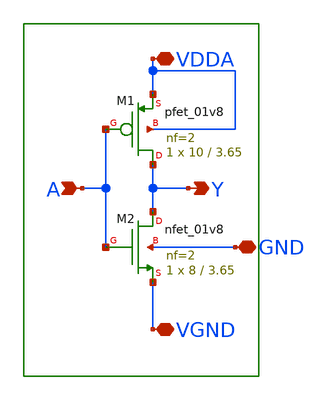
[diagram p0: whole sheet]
** sch_path: xschem/lib/main_inv.sch
**.subckt main_inv VDDA VGND A Y GND
*.iopin VDDA
*.iopin VGND
*.ipin A
*.opin Y
*.iopin GND
XM2 Y A VGND GND sky130_fd_pr__nfet_01v8 L=3.65 W=8 nf=2 ad='int((nf+1)/2) * W/nf * 0.29' as='int((nf+2)/2) * W/nf * 0.29'
+ pd='2*int((nf+1)/2) * (W/nf + 0.29)' ps='2*int((nf+2)/2) * (W/nf + 0.29)' nrd='0.29 / W' nrs='0.29 / W'
+ sa=0 sb=0 sd=0 mult=1 m=1
XM1 Y A VDDA VDDA sky130_fd_pr__pfet_01v8 L=3.65 W=10 nf=2 ad='int((nf+1)/2) * W/nf * 0.29' as='int((nf+2)/2) * W/nf * 0.29'
+ pd='2*int((nf+1)/2) * (W/nf + 0.29)' ps='2*int((nf+2)/2) * (W/nf + 0.29)' nrd='0.29 / W' nrs='0.29 / W'
+ sa=0 sb=0 sd=0 mult=1 m=1
**.ends
.end
